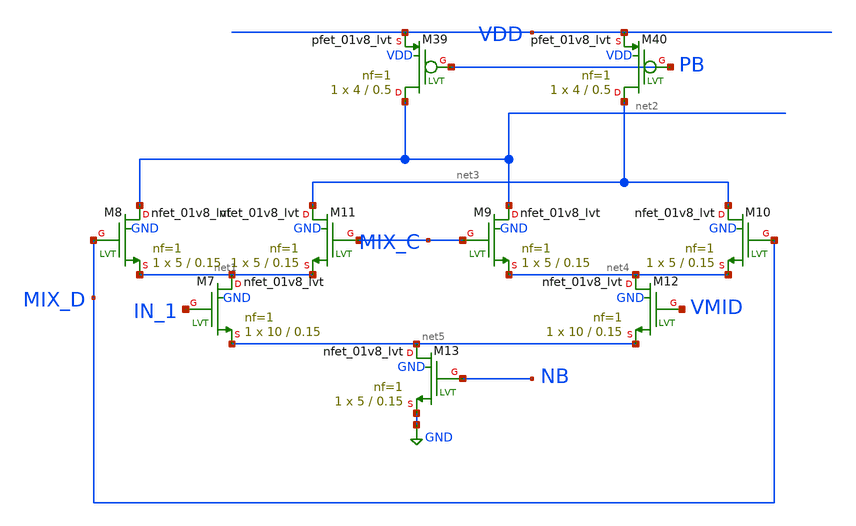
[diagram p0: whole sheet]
** sch_path: xschem/xschemwrap/gilbert.sch
**.subckt gilbert
XM7 net1 IN_1 net5 GND sky130_fd_pr__nfet_01v8_lvt L=0.15 W=10 nf=1 ad='int((1 + 1)/2) * 10 / 1 * 0.29'
+ as='int((1 + 2)/2) * 10 / 1 * 0.29' pd='2*int((1 + 1)/2) * (10 / 1 + 0.29)' ps='2*int((1 + 2)/2) * (10 / 1 + 0.29)'
+ nrd='0.29 / 10 ' nrs='0.29 / 10 ' sa=0 sb=0 sd=0 mult=1 m=1
XM8 net2 MIX_D net1 GND sky130_fd_pr__nfet_01v8_lvt L=0.15 W=5 nf=1 ad='int((1 + 1)/2) * 5 / 1 * 0.29'
+ as='int((1 + 2)/2) * 5 / 1 * 0.29' pd='2*int((1 + 1)/2) * (5 / 1 + 0.29)' ps='2*int((1 + 2)/2) * (5 / 1 + 0.29)'
+ nrd='0.29 / 5 ' nrs='0.29 / 5 ' sa=0 sb=0 sd=0 mult=1 m=1
XM9 net2 MIX_C net4 GND sky130_fd_pr__nfet_01v8_lvt L=0.15 W=5 nf=1 ad='int((1 + 1)/2) * 5 / 1 * 0.29'
+ as='int((1 + 2)/2) * 5 / 1 * 0.29' pd='2*int((1 + 1)/2) * (5 / 1 + 0.29)' ps='2*int((1 + 2)/2) * (5 / 1 + 0.29)'
+ nrd='0.29 / 5 ' nrs='0.29 / 5 ' sa=0 sb=0 sd=0 mult=1 m=1
XM10 net3 MIX_D net4 GND sky130_fd_pr__nfet_01v8_lvt L=0.15 W=5 nf=1 ad='int((1 + 1)/2) * 5 / 1 * 0.29'
+ as='int((1 + 2)/2) * 5 / 1 * 0.29' pd='2*int((1 + 1)/2) * (5 / 1 + 0.29)' ps='2*int((1 + 2)/2) * (5 / 1 + 0.29)'
+ nrd='0.29 / 5 ' nrs='0.29 / 5 ' sa=0 sb=0 sd=0 mult=1 m=1
XM11 net3 MIX_C net1 GND sky130_fd_pr__nfet_01v8_lvt L=0.15 W=5 nf=1 ad='int((1 + 1)/2) * 5 / 1 * 0.29'
+ as='int((1 + 2)/2) * 5 / 1 * 0.29' pd='2*int((1 + 1)/2) * (5 / 1 + 0.29)' ps='2*int((1 + 2)/2) * (5 / 1 + 0.29)'
+ nrd='0.29 / 5 ' nrs='0.29 / 5 ' sa=0 sb=0 sd=0 mult=1 m=1
XM12 net4 VMID net5 GND sky130_fd_pr__nfet_01v8_lvt L=0.15 W=10 nf=1 ad='int((1 + 1)/2) * 10 / 1 * 0.29'
+ as='int((1 + 2)/2) * 10 / 1 * 0.29' pd='2*int((1 + 1)/2) * (10 / 1 + 0.29)' ps='2*int((1 + 2)/2) * (10 / 1 + 0.29)'
+ nrd='0.29 / 10 ' nrs='0.29 / 10 ' sa=0 sb=0 sd=0 mult=1 m=1
XM13 net5 NB GND GND sky130_fd_pr__nfet_01v8_lvt L=0.15 W=5 nf=1 ad='int((1 + 1)/2) * 5 / 1 * 0.29' as='int((1 + 2)/2) * 5 / 1 * 0.29'
+ pd='2*int((1 + 1)/2) * (5 / 1 + 0.29)' ps='2*int((1 + 2)/2) * (5 / 1 + 0.29)' nrd='0.29 / 5 ' nrs='0.29 / 5 '
+ sa=0 sb=0 sd=0 mult=1 m=1
XM39 net2 PB VDD VDD sky130_fd_pr__pfet_01v8_lvt L=0.5 W=4 nf=1 ad='int((1 + 1)/2) * 4 / 1 * 0.29' as='int((1 + 2)/2) * 4 / 1 * 0.29'
+ pd='2*int((1 + 1)/2) * (4 / 1 + 0.29)' ps='2*int((1 + 2)/2) * (4 / 1 + 0.29)' nrd='0.29 / 4 ' nrs='0.29 / 4 '
+ sa=0 sb=0 sd=0 mult=1 m=1
XM40 net3 PB VDD VDD sky130_fd_pr__pfet_01v8_lvt L=0.5 W=4 nf=1 ad='int((1 + 1)/2) * 4 / 1 * 0.29' as='int((1 + 2)/2) * 4 / 1 * 0.29'
+ pd='2*int((1 + 1)/2) * (4 / 1 + 0.29)' ps='2*int((1 + 2)/2) * (4 / 1 + 0.29)' nrd='0.29 / 4 ' nrs='0.29 / 4 '
+ sa=0 sb=0 sd=0 mult=1 m=1
**.ends
.GLOBAL GND
.end
